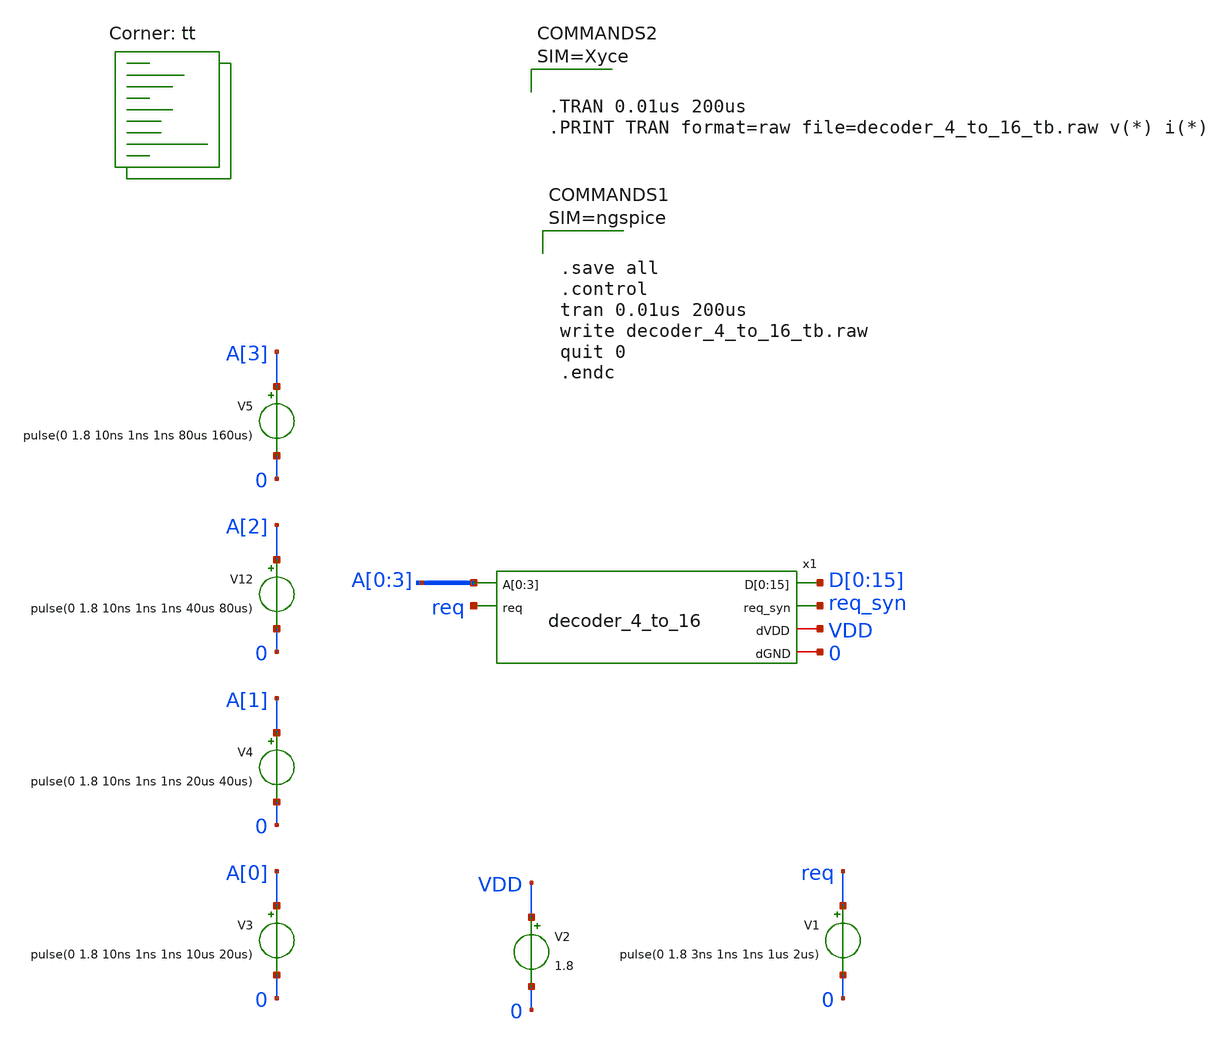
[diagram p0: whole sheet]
** sch_path: design/xschem/decoder_4_to_16_tb.sch
**.subckt decoder_4_to_16_tb
V12 A[2] 0 pulse(0 1.8 10ns 1ns 1ns 40us 80us)
V5 A[3] 0 pulse(0 1.8 10ns 1ns 1ns 80us 160us)
V3 A[0] 0 pulse(0 1.8 10ns 1ns 1ns 10us 20us)
V4 A[1] 0 pulse(0 1.8 10ns 1ns 1ns 20us 40us)
V2 VDD 0 1.8
V1 req 0 pulse(0 1.8 3ns 1ns 1ns 1us 2us)
x1 A[0] A[1] A[2] A[3] D[0] D[1] D[2] D[3] D[4] D[5] D[6] D[7] D[8] D[9] D[10] D[11] D[12] D[13]
+ D[14] D[15] req req_syn VDD 0 decoder_4_to_16
**** begin user architecture code


* Standard cell simulation files
.include $::SKYWATER_STDCELLS/sky130_fd_sc_hd.spice




.save all
.control
tran 0.01us 200us
write decoder_4_to_16_tb.raw
quit 0
.endc






.lib $::SKYWATER_MODELS/sky130.lib.spice tt
**** end user architecture code
**.ends

* expanding   symbol:  decoder_4_to_16.sym # of pins=6
** sym_path: design/xschem/decoder_4_to_16.sym
** sch_path: design/xschem/decoder_4_to_16.sch
.subckt decoder_4_to_16 A[0] A[1] A[2] A[3] D[0] D[1] D[2] D[3] D[4] D[5] D[6] D[7] D[8] D[9] D[10]
+ D[11] D[12] D[13] D[14] D[15] req req_syn dVDD dGND
*.ipin A[0],A[1],A[2],A[3]
*.ipin req
*.opin D[0],D[1],D[2],D[3],D[4],D[5],D[6],D[7],D[8],D[9],D[10],D[11],D[12],D[13],D[14],D[15]
*.opin req_syn
*.iopin dVDD
*.iopin dGND
x21 req dGND dGND dVDD dVDD net5 sky130_fd_sc_hd__inv_1
x22 net5 dGND dGND dVDD dVDD net6 sky130_fd_sc_hd__inv_1
x23 net6 dGND dGND dVDD dVDD net7 sky130_fd_sc_hd__inv_1
x24 net7 dGND dGND dVDD dVDD req_syn sky130_fd_sc_hd__inv_1
x20 A[3] A[2] A[1] A[0] dGND dGND dVDD dVDD D[15] sky130_fd_sc_hd__and4_1
x19 A[3] A[2] A[1] net4 dGND dGND dVDD dVDD D[14] sky130_fd_sc_hd__and4_1
x18 A[3] A[2] net3 A[0] dGND dGND dVDD dVDD D[13] sky130_fd_sc_hd__and4_1
x17 A[3] A[2] net3 net4 dGND dGND dVDD dVDD D[12] sky130_fd_sc_hd__and4_1
x16 A[3] net2 A[1] A[0] dGND dGND dVDD dVDD D[11] sky130_fd_sc_hd__and4_1
x15 A[3] net2 A[1] net4 dGND dGND dVDD dVDD D[10] sky130_fd_sc_hd__and4_1
x13 A[3] net2 net3 A[0] dGND dGND dVDD dVDD D[9] sky130_fd_sc_hd__and4_1
x4 A[3] net2 net3 net4 dGND dGND dVDD dVDD D[8] sky130_fd_sc_hd__and4_1
x5 net1 A[2] A[1] A[0] dGND dGND dVDD dVDD D[7] sky130_fd_sc_hd__and4_1
x6 net1 A[2] A[1] net4 dGND dGND dVDD dVDD D[6] sky130_fd_sc_hd__and4_1
x8 net1 A[2] net3 net4 dGND dGND dVDD dVDD D[4] sky130_fd_sc_hd__and4_1
x9 net1 net2 A[1] net4 dGND dGND dVDD dVDD D[2] sky130_fd_sc_hd__and4_1
x10 net1 net2 net3 net4 dGND dGND dVDD dVDD D[0] sky130_fd_sc_hd__and4_1
x11 net1 net2 net3 A[0] dGND dGND dVDD dVDD D[1] sky130_fd_sc_hd__and4_1
x12 net1 net2 A[1] A[0] dGND dGND dVDD dVDD D[3] sky130_fd_sc_hd__and4_1
x14 net1 A[2] net3 A[0] dGND dGND dVDD dVDD D[5] sky130_fd_sc_hd__and4_1
x1 A[3] dGND dGND dVDD dVDD net1 sky130_fd_sc_hd__inv_4
x2 A[2] dGND dGND dVDD dVDD net2 sky130_fd_sc_hd__inv_4
x3 A[1] dGND dGND dVDD dVDD net3 sky130_fd_sc_hd__inv_4
x7 A[0] dGND dGND dVDD dVDD net4 sky130_fd_sc_hd__inv_4
.ends

.end
